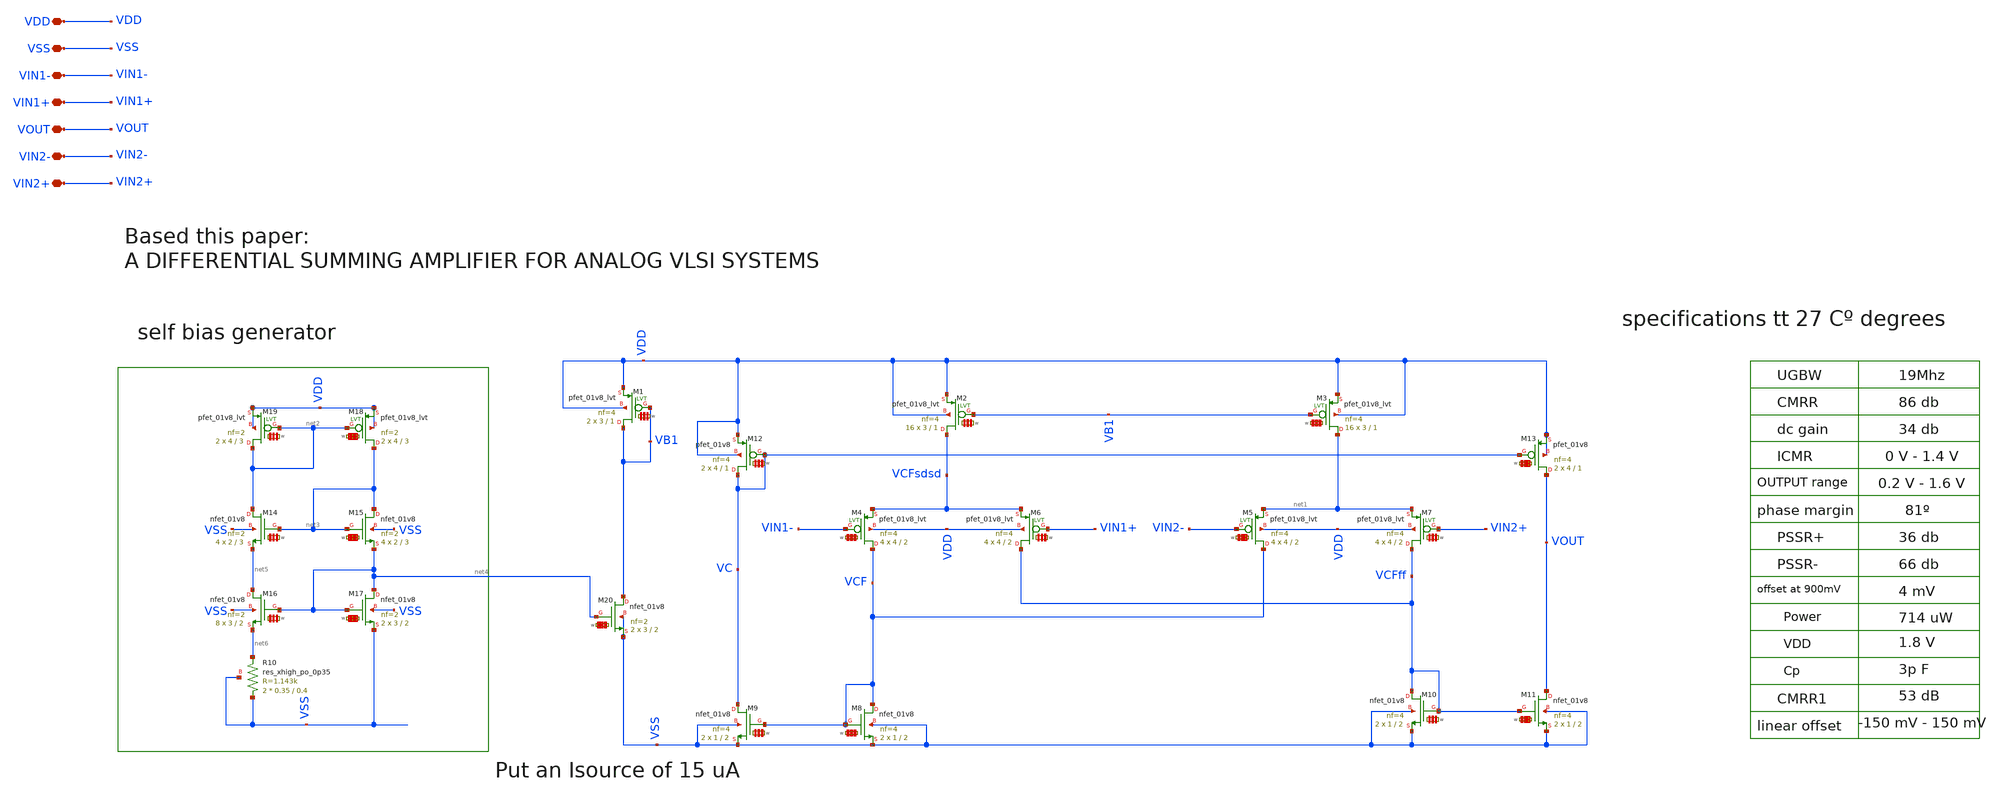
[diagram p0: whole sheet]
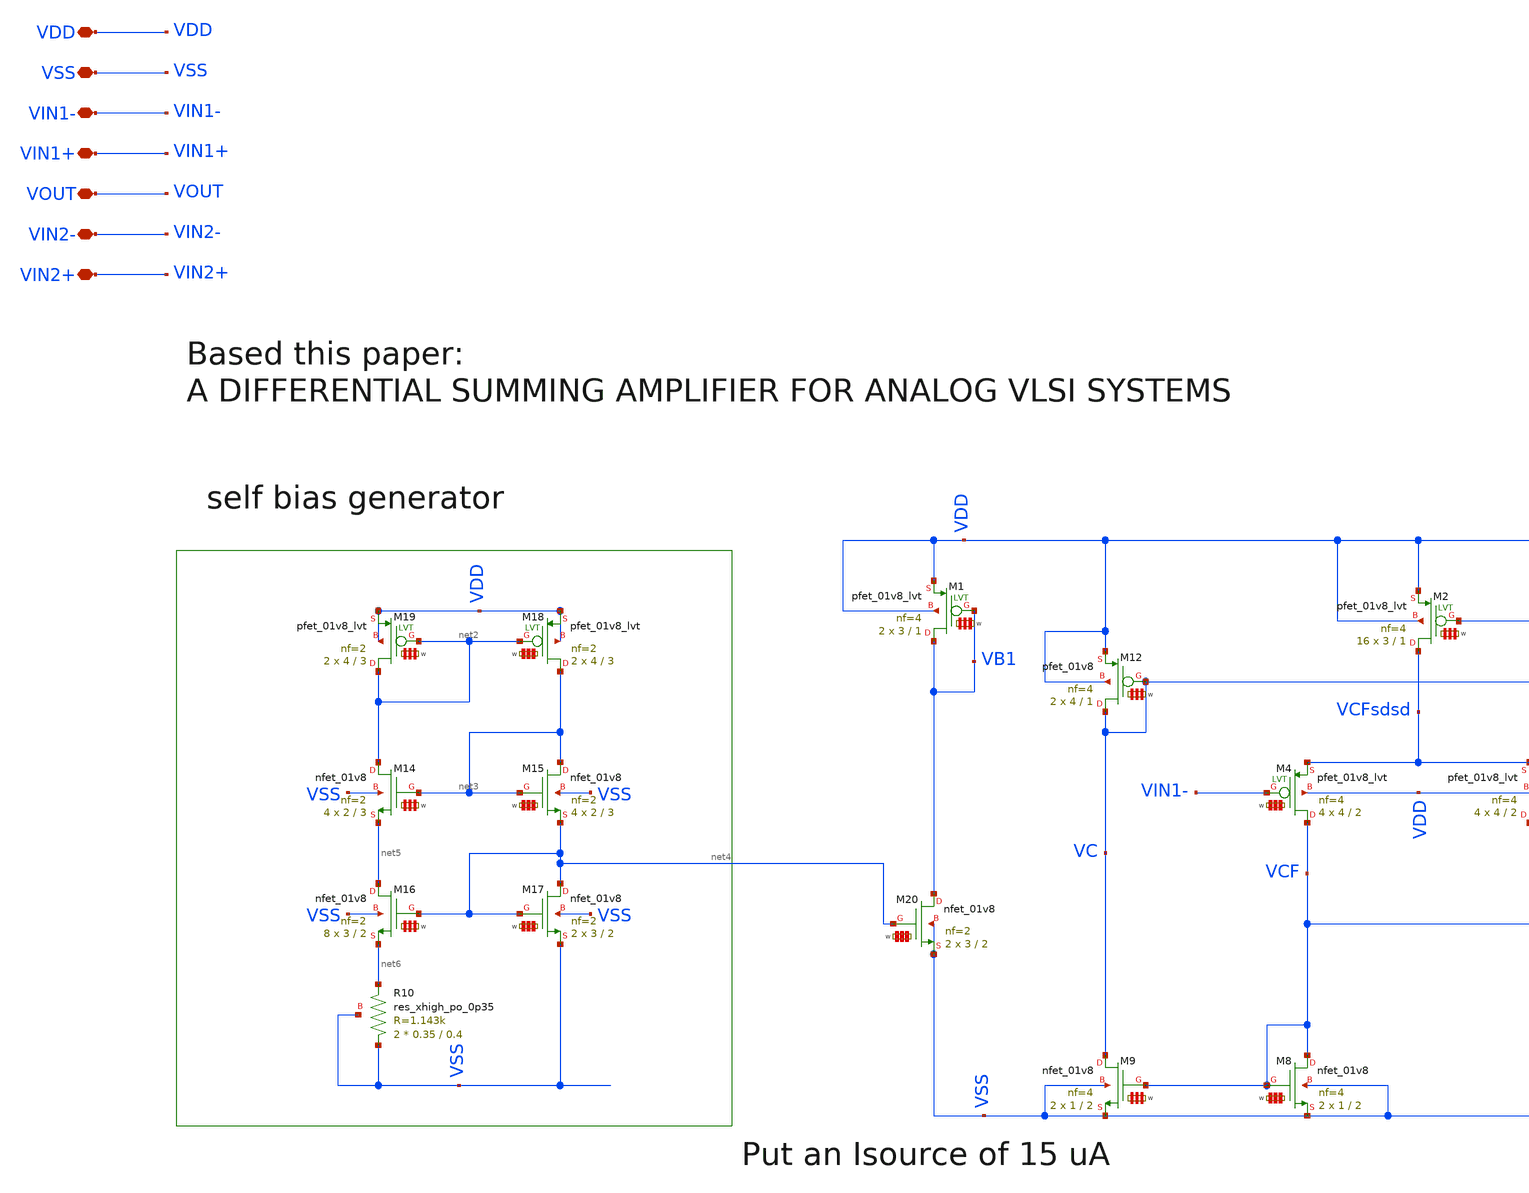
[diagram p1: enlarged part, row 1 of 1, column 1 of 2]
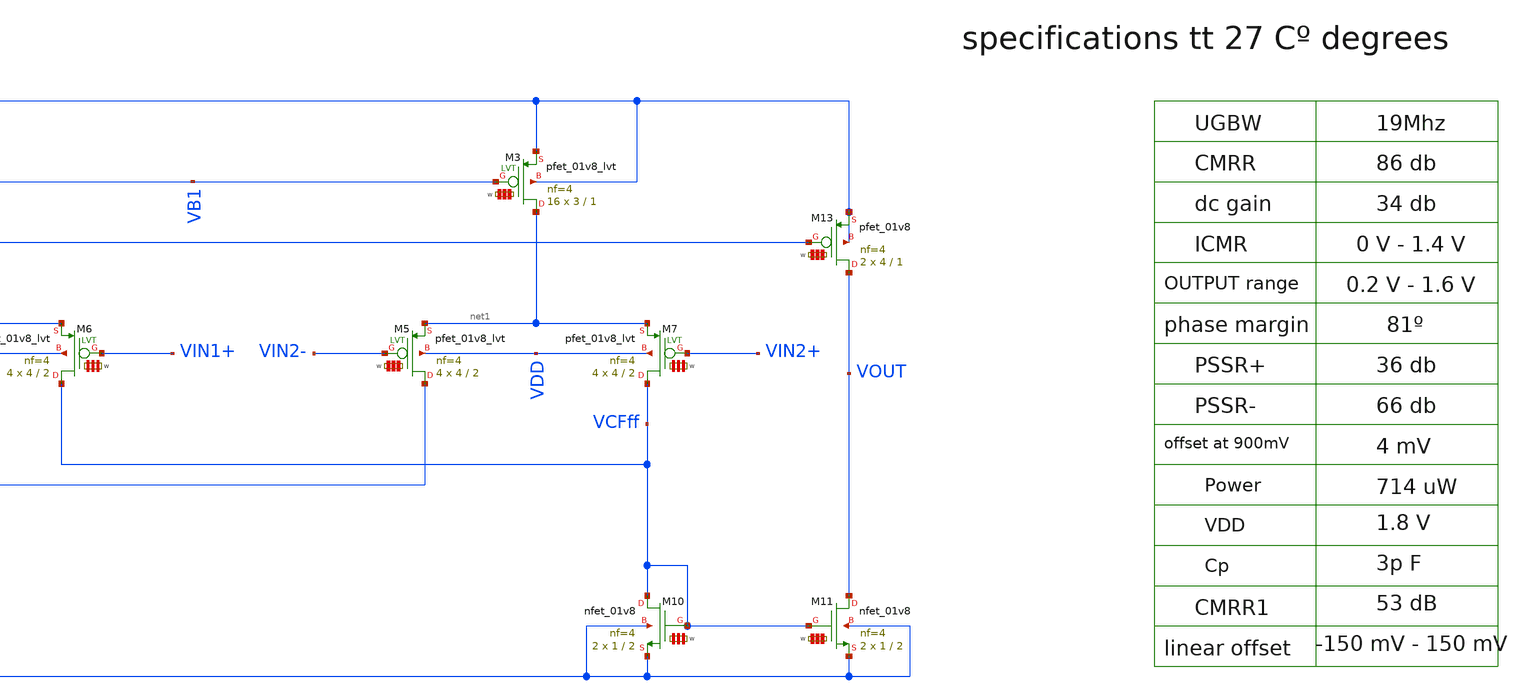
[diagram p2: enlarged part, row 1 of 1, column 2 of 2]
** sch_path: LIB/Sky130A/DDA/DDA001_PMOS_1.8_sky130A .sch
**.subckt DDA001_PMOS_1.8_sky130A  VDD VSS VIN1- VIN1+ VOUT VIN2- VIN2+
*.iopin VDD
*.iopin VSS
*.iopin VIN1-
*.iopin VIN1+
*.iopin VOUT
*.iopin VIN2-
*.iopin VIN2+
XM1 VB1 VB1 VDD VDD sky130_fd_pr__pfet_01v8_lvt L=1 W='3 * 4 ' nf=4 ad='int((4 + 1)/2) * 3 / 4 * 0.29'
+ as='int((4 + 2)/2) * 3 / 4 * 0.29' pd='2*int((4 + 1)/2) * (3 / 4 + 0.29)' ps='2*int((4 + 2)/2) * (3 / 4 + 0.29)'
+ nrd='0.29 / 3 ' nrs='0.29 / 3 ' sa=0 sb=0 sd=0 mult=2 m=2
XM2 VCFsdsd VB1 VDD VDD sky130_fd_pr__pfet_01v8_lvt L=1 W='3 * 4 ' nf=4 ad='int((4 + 1)/2) * 3 / 4 * 0.29'
+ as='int((4 + 2)/2) * 3 / 4 * 0.29' pd='2*int((4 + 1)/2) * (3 / 4 + 0.29)' ps='2*int((4 + 2)/2) * (3 / 4 + 0.29)'
+ nrd='0.29 / 3 ' nrs='0.29 / 3 ' sa=0 sb=0 sd=0 mult=16 m=16
XM3 net1 VB1 VDD VDD sky130_fd_pr__pfet_01v8_lvt L=1 W='3 * 4 ' nf=4 ad='int((4 + 1)/2) * 3 / 4 * 0.29'
+ as='int((4 + 2)/2) * 3 / 4 * 0.29' pd='2*int((4 + 1)/2) * (3 / 4 + 0.29)' ps='2*int((4 + 2)/2) * (3 / 4 + 0.29)'
+ nrd='0.29 / 3 ' nrs='0.29 / 3 ' sa=0 sb=0 sd=0 mult=16 m=16
XM4 VCF VIN1- VCFsdsd VDD sky130_fd_pr__pfet_01v8_lvt L=2 W='4 * 4 ' nf=4 ad='int((4 + 1)/2) * 4 / 4 * 0.29'
+ as='int((4 + 2)/2) * 4 / 4 * 0.29' pd='2*int((4 + 1)/2) * (4 / 4 + 0.29)' ps='2*int((4 + 2)/2) * (4 / 4 + 0.29)'
+ nrd='0.29 / 4 ' nrs='0.29 / 4 ' sa=0 sb=0 sd=0 mult=4 m=4
XM8 VCF VCF VSS VSS sky130_fd_pr__nfet_01v8 L=2 W='1 * 4 ' nf=4 ad='int((4 + 1)/2) * 1 / 4 * 0.29' as='int((4 + 2)/2) * 1 / 4 * 0.29'
+ pd='2*int((4 + 1)/2) * (1 / 4 + 0.29)' ps='2*int((4 + 2)/2) * (1 / 4 + 0.29)' nrd='0.29 / 1 ' nrs='0.29 / 1 '
+ sa=0 sb=0 sd=0 mult=2 m=2
XM9 VC VCF VSS VSS sky130_fd_pr__nfet_01v8 L=2 W='1 * 4 ' nf=4 ad='int((4 + 1)/2) * 1 / 4 * 0.29' as='int((4 + 2)/2) * 1 / 4 * 0.29'
+ pd='2*int((4 + 1)/2) * (1 / 4 + 0.29)' ps='2*int((4 + 2)/2) * (1 / 4 + 0.29)' nrd='0.29 / 1 ' nrs='0.29 / 1 '
+ sa=0 sb=0 sd=0 mult=2 m=2
XM10 VCFff VCFff VSS VSS sky130_fd_pr__nfet_01v8 L=2 W='1 * 4 ' nf=4 ad='int((4 + 1)/2) * 1 / 4 * 0.29'
+ as='int((4 + 2)/2) * 1 / 4 * 0.29' pd='2*int((4 + 1)/2) * (1 / 4 + 0.29)' ps='2*int((4 + 2)/2) * (1 / 4 + 0.29)'
+ nrd='0.29 / 1 ' nrs='0.29 / 1 ' sa=0 sb=0 sd=0 mult=2 m=2
XM11 VOUT VCFff VSS VSS sky130_fd_pr__nfet_01v8 L=2 W='1 * 4 ' nf=4 ad='int((4 + 1)/2) * 1 / 4 * 0.29'
+ as='int((4 + 2)/2) * 1 / 4 * 0.29' pd='2*int((4 + 1)/2) * (1 / 4 + 0.29)' ps='2*int((4 + 2)/2) * (1 / 4 + 0.29)'
+ nrd='0.29 / 1 ' nrs='0.29 / 1 ' sa=0 sb=0 sd=0 mult=2 m=2
XM12 VC VC VDD VDD sky130_fd_pr__pfet_01v8 L=1 W='4 * 4 ' nf=4 ad= as='int((4 + 2)/2) * 4 * 0.29' pd='2*int((4 + 1)/2) * (4 + 0.29)'
+ ps='2*int((4 + 2)/2) * (4 + 0.29)' nrd='0.29 / 4 / 4 ' nrs='0.29 / 4 / 4 ' sa=0 sb=0 sd=0 mult=2 m=2
XM13 VOUT VC VDD VDD sky130_fd_pr__pfet_01v8 L=1 W='4 * 4 ' nf=4 ad= as='int((4 + 2)/2) * 4 * 0.29' pd='2*int((4 + 1)/2) * (4 + 0.29)'
+ ps='2*int((4 + 2)/2) * (4 + 0.29)' nrd='0.29 / 4 / 4 ' nrs='0.29 / 4 / 4 ' sa=0 sb=0 sd=0 mult=2 m=2
XM5 VCF VIN2- net1 VDD sky130_fd_pr__pfet_01v8_lvt L=2 W='4 * 4 ' nf=4 ad='int((4 + 1)/2) * 4 / 4 * 0.29'
+ as='int((4 + 2)/2) * 4 / 4 * 0.29' pd='2*int((4 + 1)/2) * (4 / 4 + 0.29)' ps='2*int((4 + 2)/2) * (4 / 4 + 0.29)'
+ nrd='0.29 / 4 ' nrs='0.29 / 4 ' sa=0 sb=0 sd=0 mult=4 m=4
XM6 VCFff VIN1+ VCFsdsd VDD sky130_fd_pr__pfet_01v8_lvt L=2 W='4 * 4 ' nf=4 ad='int((4 + 1)/2) * 4 / 4 * 0.29'
+ as='int((4 + 2)/2) * 4 / 4 * 0.29' pd='2*int((4 + 1)/2) * (4 / 4 + 0.29)' ps='2*int((4 + 2)/2) * (4 / 4 + 0.29)'
+ nrd='0.29 / 4 ' nrs='0.29 / 4 ' sa=0 sb=0 sd=0 mult=4 m=4
XM7 VCFff VIN2+ net1 VDD sky130_fd_pr__pfet_01v8_lvt L=2 W='4 * 4 ' nf=4 ad='int((4 + 1)/2) * 4 / 4 * 0.29'
+ as='int((4 + 2)/2) * 4 / 4 * 0.29' pd='2*int((4 + 1)/2) * (4 / 4 + 0.29)' ps='2*int((4 + 2)/2) * (4 / 4 + 0.29)'
+ nrd='0.29 / 4 ' nrs='0.29 / 4 ' sa=0 sb=0 sd=0 mult=4 m=4
XR10 VSS net6 VSS sky130_fd_pr__res_xhigh_po_0p35 L=0.4 mult=2 m=2
XM14 net2 net3 net5 VSS sky130_fd_pr__nfet_01v8 L=3 W='2 * 2 ' nf=2 ad='int((2 + 1)/2) * 2 / 2 * 0.29'
+ as='int((2 + 2)/2) * 2 / 2 * 0.29' pd='2*int((2 + 1)/2) * (2 / 2 + 0.29)' ps='2*int((2 + 2)/2) * (2 / 2 + 0.29)'
+ nrd='0.29 / 2 ' nrs='0.29 / 2 ' sa=0 sb=0 sd=0 mult=4 m=4
XM15 net3 net3 net4 VSS sky130_fd_pr__nfet_01v8 L=3 W='2 * 2 ' nf=2 ad='int((2 + 1)/2) * 2 / 2 * 0.29'
+ as='int((2 + 2)/2) * 2 / 2 * 0.29' pd='2*int((2 + 1)/2) * (2 / 2 + 0.29)' ps='2*int((2 + 2)/2) * (2 / 2 + 0.29)'
+ nrd='0.29 / 2 ' nrs='0.29 / 2 ' sa=0 sb=0 sd=0 mult=4 m=4
XM16 net5 net4 net6 VSS sky130_fd_pr__nfet_01v8 L=2 W='3 * 2 ' nf=2 ad='int((2 + 1)/2) * 3 / 2 * 0.29'
+ as='int((2 + 2)/2) * 3 / 2 * 0.29' pd='2*int((2 + 1)/2) * (3 / 2 + 0.29)' ps='2*int((2 + 2)/2) * (3 / 2 + 0.29)'
+ nrd='0.29 / 3 ' nrs='0.29 / 3 ' sa=0 sb=0 sd=0 mult=8 m=8
XM17 net4 net4 VSS VSS sky130_fd_pr__nfet_01v8 L=2 W='3 * 2 ' nf=2 ad='int((2 + 1)/2) * 3 / 2 * 0.29'
+ as='int((2 + 2)/2) * 3 / 2 * 0.29' pd='2*int((2 + 1)/2) * (3 / 2 + 0.29)' ps='2*int((2 + 2)/2) * (3 / 2 + 0.29)'
+ nrd='0.29 / 3 ' nrs='0.29 / 3 ' sa=0 sb=0 sd=0 mult=2 m=2
XM18 net3 net2 VDD VDD sky130_fd_pr__pfet_01v8_lvt L=3 W='4 * 2 ' nf=2 ad='int((2 + 1)/2) * 4 / 2 * 0.29'
+ as='int((2 + 2)/2) * 4 / 2 * 0.29' pd='2*int((2 + 1)/2) * (4 / 2 + 0.29)' ps='2*int((2 + 2)/2) * (4 / 2 + 0.29)'
+ nrd='0.29 / 4 ' nrs='0.29 / 4 ' sa=0 sb=0 sd=0 mult=2 m=2
XM19 net2 net2 VDD VDD sky130_fd_pr__pfet_01v8_lvt L=3 W='4 * 2 ' nf=2 ad='int((2 + 1)/2) * 4 / 2 * 0.29'
+ as='int((2 + 2)/2) * 4 / 2 * 0.29' pd='2*int((2 + 1)/2) * (4 / 2 + 0.29)' ps='2*int((2 + 2)/2) * (4 / 2 + 0.29)'
+ nrd='0.29 / 4 ' nrs='0.29 / 4 ' sa=0 sb=0 sd=0 mult=2 m=2
XM20 VB1 net4 VSS VSS sky130_fd_pr__nfet_01v8 L=2 W='3 * 2 ' nf=2 ad='int((2 + 1)/2) * 3 / 2 * 0.29'
+ as='int((2 + 2)/2) * 3 / 2 * 0.29' pd='2*int((2 + 1)/2) * (3 / 2 + 0.29)' ps='2*int((2 + 2)/2) * (3 / 2 + 0.29)'
+ nrd='0.29 / 3 ' nrs='0.29 / 3 ' sa=0 sb=0 sd=0 mult=2 m=2
**.ends
.end
